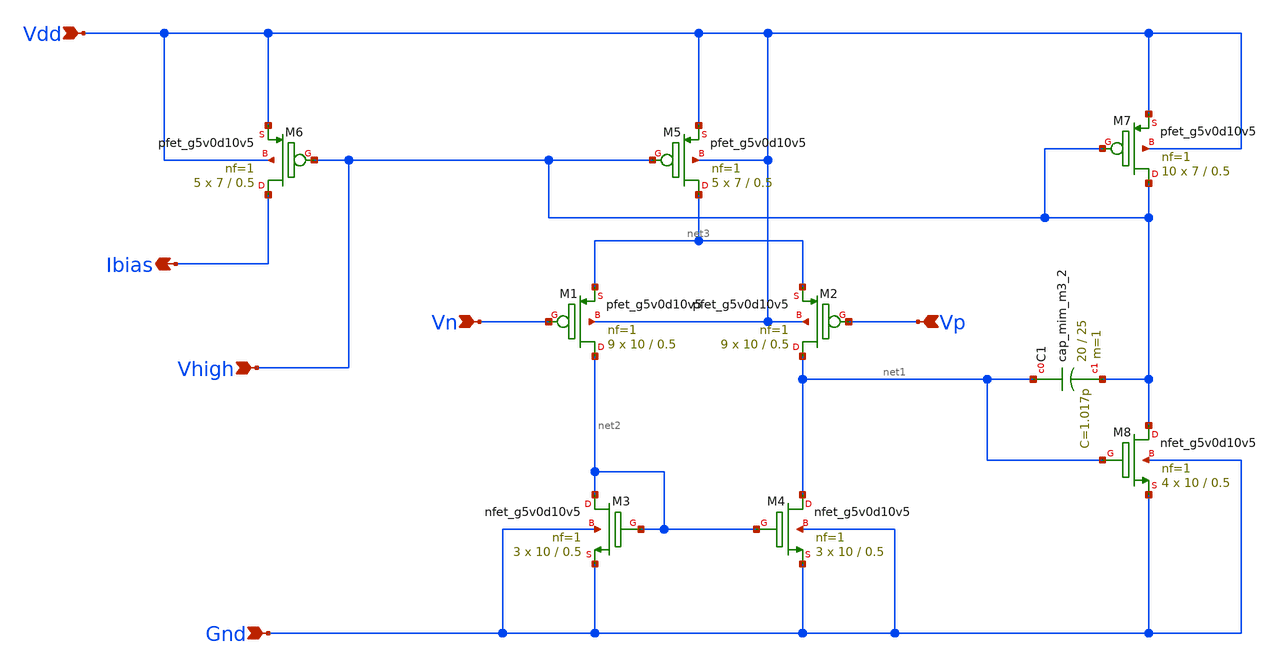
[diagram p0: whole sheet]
** sch_path: Analog_blocks/Analog_Blocks/Bandgap/Schematics/BGR1.8v/Bandgap1.8v_OTA.sch
**.subckt Bandgap1.8v_OTA Ibias Vhigh Vdd Gnd Vp Vn
*.opin Ibias
*.ipin Vhigh
*.ipin Vdd
*.ipin Gnd
*.ipin Vp
*.ipin Vn
XM6 Ibias Vhigh Vdd Vdd sky130_fd_pr__pfet_g5v0d10v5 L=0.5 W=7 nf=1 ad='int((nf+1)/2) * W/nf * 0.29'
+ as='int((nf+2)/2) * W/nf * 0.29' pd='2*int((nf+1)/2) * (W/nf + 0.29)' ps='2*int((nf+2)/2) * (W/nf + 0.29)'
+ nrd='0.29 / W' nrs='0.29 / W' sa=0 sb=0 sd=0 mult=5 m=5
XM5 net3 Vhigh Vdd Vdd sky130_fd_pr__pfet_g5v0d10v5 L=0.5 W=7 nf=1 ad='int((nf+1)/2) * W/nf * 0.29' as='int((nf+2)/2) * W/nf * 0.29'
+ pd='2*int((nf+1)/2) * (W/nf + 0.29)' ps='2*int((nf+2)/2) * (W/nf + 0.29)' nrd='0.29 / W' nrs='0.29 / W'
+ sa=0 sb=0 sd=0 mult=5 m=5
XM1 net2 Vn net3 Vdd sky130_fd_pr__pfet_g5v0d10v5 L=0.5 W=10 nf=1 ad='int((nf+1)/2) * W/nf * 0.29' as='int((nf+2)/2) * W/nf * 0.29'
+ pd='2*int((nf+1)/2) * (W/nf + 0.29)' ps='2*int((nf+2)/2) * (W/nf + 0.29)' nrd='0.29 / W' nrs='0.29 / W'
+ sa=0 sb=0 sd=0 mult=9 m=9
XM8 Vhigh net1 Gnd Gnd sky130_fd_pr__nfet_g5v0d10v5 L=0.5 W=10 nf=1 ad='int((nf+1)/2) * W/nf * 0.29'
+ as='int((nf+2)/2) * W/nf * 0.29' pd='2*int((nf+1)/2) * (W/nf + 0.29)' ps='2*int((nf+2)/2) * (W/nf + 0.29)'
+ nrd='0.29 / W' nrs='0.29 / W' sa=0 sb=0 sd=0 mult=4 m=4
XM4 net1 net2 Gnd Gnd sky130_fd_pr__nfet_g5v0d10v5 L=0.5 W=10 nf=1 ad='int((nf+1)/2) * W/nf * 0.29' as='int((nf+2)/2) * W/nf * 0.29'
+ pd='2*int((nf+1)/2) * (W/nf + 0.29)' ps='2*int((nf+2)/2) * (W/nf + 0.29)' nrd='0.29 / W' nrs='0.29 / W'
+ sa=0 sb=0 sd=0 mult=3 m=3
XM3 net2 net2 Gnd Gnd sky130_fd_pr__nfet_g5v0d10v5 L=0.5 W=10 nf=1 ad='int((nf+1)/2) * W/nf * 0.29' as='int((nf+2)/2) * W/nf * 0.29'
+ pd='2*int((nf+1)/2) * (W/nf + 0.29)' ps='2*int((nf+2)/2) * (W/nf + 0.29)' nrd='0.29 / W' nrs='0.29 / W'
+ sa=0 sb=0 sd=0 mult=3 m=3
XC1 net1 Vhigh sky130_fd_pr__cap_mim_m3_2 W=20 L=25 MF=1 m=1
XM2 net1 Vp net3 Vdd sky130_fd_pr__pfet_g5v0d10v5 L=0.5 W=10 nf=1 ad='int((nf+1)/2) * W/nf * 0.29' as='int((nf+2)/2) * W/nf * 0.29'
+ pd='2*int((nf+1)/2) * (W/nf + 0.29)' ps='2*int((nf+2)/2) * (W/nf + 0.29)' nrd='0.29 / W' nrs='0.29 / W'
+ sa=0 sb=0 sd=0 mult=9 m=9
XM7 Vhigh Vhigh Vdd Vdd sky130_fd_pr__pfet_g5v0d10v5 L=0.5 W=7 nf=1 ad='int((nf+1)/2) * W/nf * 0.29'
+ as='int((nf+2)/2) * W/nf * 0.29' pd='2*int((nf+1)/2) * (W/nf + 0.29)' ps='2*int((nf+2)/2) * (W/nf + 0.29)'
+ nrd='0.29 / W' nrs='0.29 / W' sa=0 sb=0 sd=0 mult=10 m=10
**.ends
.end
